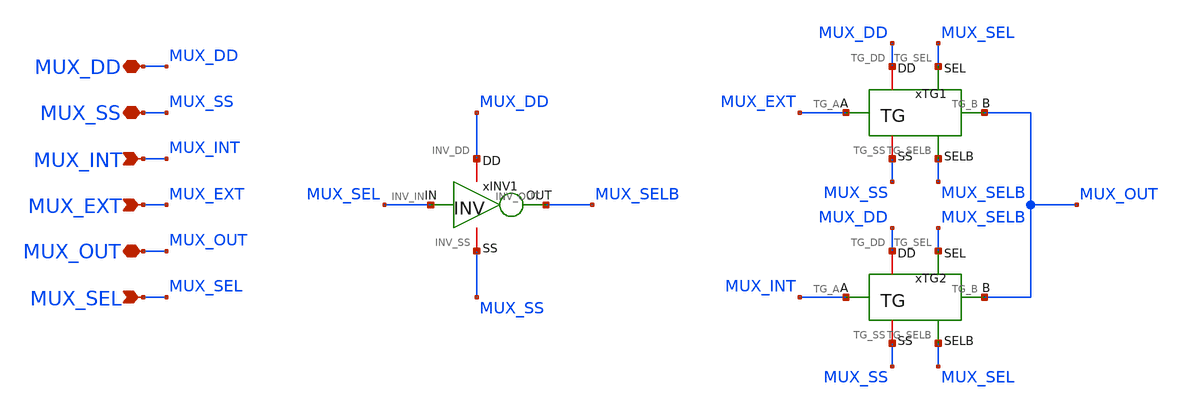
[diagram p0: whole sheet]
** sch_path: Design_Files/IC Design/Schematic/DIGITAL_BLOCKS/MUX/MUX.sch
**.subckt MUX MUX_DD MUX_SS MUX_INT MUX_OUT MUX_EXT MUX_SEL
*.iopin MUX_DD
*.iopin MUX_SS
*.ipin MUX_INT
*.iopin MUX_OUT
*.ipin MUX_EXT
*.ipin MUX_SEL
xINV1 MUX_DD MUX_SS MUX_SEL MUX_SELB INV
xTG1 MUX_DD MUX_SS MUX_EXT MUX_OUT MUX_SEL MUX_SELB TG
xTG2 MUX_DD MUX_SS MUX_INT MUX_OUT MUX_SELB MUX_SEL TG
**.ends

* expanding   symbol:  ECG_Acquisition_IC/Design_Files/IC
*+ Design/Schematic/DIGITAL_BLOCKS/INV/INV.sym # of pins=4
** sym_path: Design_Files/IC Design/Schematic/INV/INV.sym
** sch_path: Design_Files/IC Design/Schematic/INV/INV.sch
.subckt INV INV_DD INV_SS INV_IN INV_OUT
*.iopin INV_DD
*.iopin INV_SS
*.ipin INV_IN
*.opin INV_OUT
XMINVP INV_OUT INV_IN INV_DD INV_DD pfet_03v3 L=0.5u W=2u nf=1 ad='int((nf+1)/2) * W/nf * 0.18u' as='int((nf+2)/2) * W/nf * 0.18u'
+ pd='2*int((nf+1)/2) * (W/nf + 0.18u)' ps='2*int((nf+2)/2) * (W/nf + 0.18u)' nrd='0.18u / W' nrs='0.18u / W'
+ sa=0 sb=0 sd=0 m=1
XMINVN INV_OUT INV_IN INV_SS INV_SS nfet_03v3 L=0.5u W=1u nf=1 ad='int((nf+1)/2) * W/nf * 0.18u' as='int((nf+2)/2) * W/nf * 0.18u'
+ pd='2*int((nf+1)/2) * (W/nf + 0.18u)' ps='2*int((nf+2)/2) * (W/nf + 0.18u)' nrd='0.18u / W' nrs='0.18u / W'
+ sa=0 sb=0 sd=0 m=1
.ends


* expanding   symbol:  ECG_Acquisition_IC/Design_Files/IC Design/Schematic/DIGITAL_BLOCKS/TG/TG.sym
*+ # of pins=6
** sym_path: Design_Files/IC Design/Schematic/TG/TG.sym
** sch_path: Design_Files/IC Design/Schematic/TG/TG.sch
.subckt TG TG_DD TG_SS TG_A TG_B TG_SEL TG_SELB
*.iopin TG_DD
*.iopin TG_SS
*.iopin TG_A
*.iopin TG_B
*.ipin TG_SEL
*.ipin TG_SELB
XMTGP TG_B TG_SELB TG_A TG_DD pfet_03v3 L=0.5u W=40u nf=1 ad='int((nf+1)/2) * W/nf * 0.18u' as='int((nf+2)/2) * W/nf * 0.18u'
+ pd='2*int((nf+1)/2) * (W/nf + 0.18u)' ps='2*int((nf+2)/2) * (W/nf + 0.18u)' nrd='0.18u / W' nrs='0.18u / W'
+ sa=0 sb=0 sd=0 m=1
XMTGN TG_A TG_SEL TG_B TG_SS nfet_03v3 L=0.5u W=20u nf=1 ad='int((nf+1)/2) * W/nf * 0.18u' as='int((nf+2)/2) * W/nf * 0.18u'
+ pd='2*int((nf+1)/2) * (W/nf + 0.18u)' ps='2*int((nf+2)/2) * (W/nf + 0.18u)' nrd='0.18u / W' nrs='0.18u / W'
+ sa=0 sb=0 sd=0 m=1
.ends

.end
